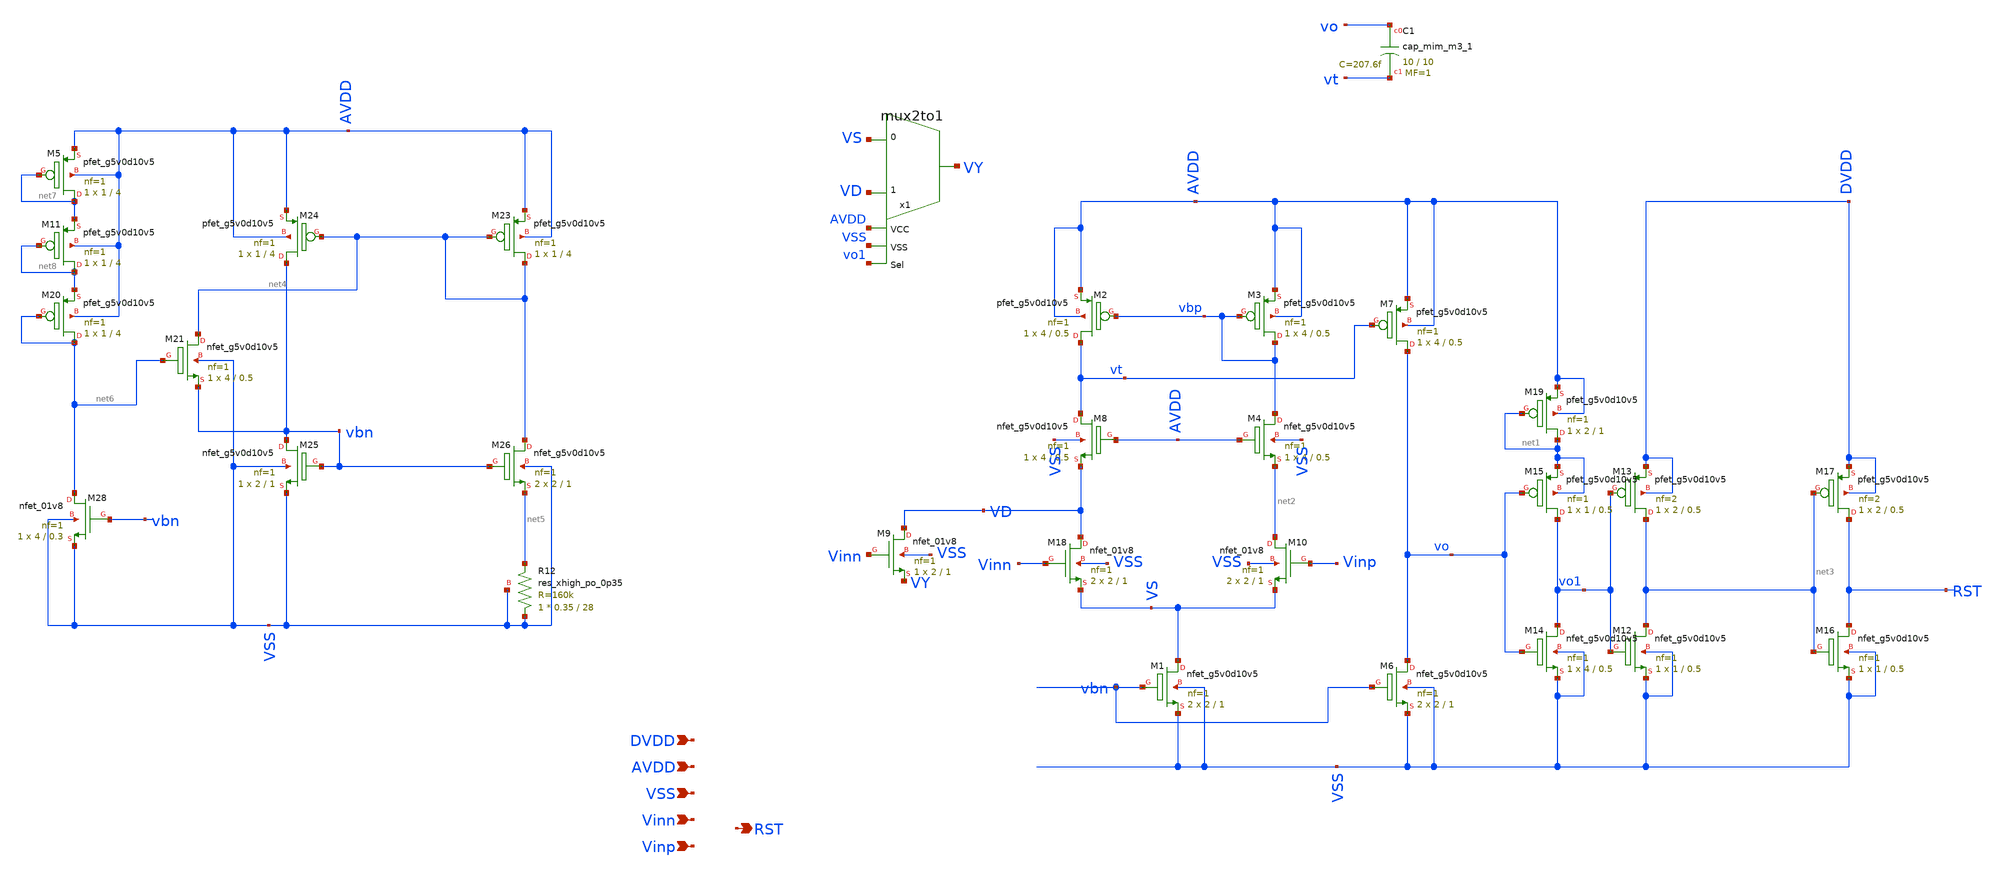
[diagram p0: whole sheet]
** sch_path: xschem/comparator_final_dev.sch
**.subckt comparator_final_dev AVDD RST VSS Vinn Vinp DVDD
*.ipin AVDD
*.opin RST
*.ipin VSS
*.ipin Vinn
*.ipin Vinp
*.ipin DVDD
XM1 VS vbn VSS VSS sky130_fd_pr__nfet_g5v0d10v5 L=1 W=2 nf=1 ad='int((nf+1)/2) * W/nf * 0.29' as='int((nf+2)/2) * W/nf * 0.29'
+ pd='2*int((nf+1)/2) * (W/nf + 0.29)' ps='2*int((nf+2)/2) * (W/nf + 0.29)' nrd='0.29 / W' nrs='0.29 / W'
+ sa=0 sb=0 sd=0 mult=2 m=2
XM3 vbp vbp AVDD AVDD sky130_fd_pr__pfet_g5v0d10v5 L=0.5 W=4 nf=1 ad='int((nf+1)/2) * W/nf * 0.29' as='int((nf+2)/2) * W/nf * 0.29'
+ pd='2*int((nf+1)/2) * (W/nf + 0.29)' ps='2*int((nf+2)/2) * (W/nf + 0.29)' nrd='0.29 / W' nrs='0.29 / W'
+ sa=0 sb=0 sd=0 mult=1 m=1
XM2 vt vbp AVDD AVDD sky130_fd_pr__pfet_g5v0d10v5 L=0.5 W=4 nf=1 ad='int((nf+1)/2) * W/nf * 0.29' as='int((nf+2)/2) * W/nf * 0.29'
+ pd='2*int((nf+1)/2) * (W/nf + 0.29)' ps='2*int((nf+2)/2) * (W/nf + 0.29)' nrd='0.29 / W' nrs='0.29 / W'
+ sa=0 sb=0 sd=0 mult=1 m=1
XM7 vo vt AVDD AVDD sky130_fd_pr__pfet_g5v0d10v5 L=0.5 W=4 nf=1 ad='int((nf+1)/2) * W/nf * 0.29' as='int((nf+2)/2) * W/nf * 0.29'
+ pd='2*int((nf+1)/2) * (W/nf + 0.29)' ps='2*int((nf+2)/2) * (W/nf + 0.29)' nrd='0.29 / W' nrs='0.29 / W'
+ sa=0 sb=0 sd=0 mult=1 m=1
x1 VD VS VY AVDD VSS vo1 mux2to1
XM6 vo vbn VSS VSS sky130_fd_pr__nfet_g5v0d10v5 L=1 W=2 nf=1 ad='int((nf+1)/2) * W/nf * 0.29' as='int((nf+2)/2) * W/nf * 0.29'
+ pd='2*int((nf+1)/2) * (W/nf + 0.29)' ps='2*int((nf+2)/2) * (W/nf + 0.29)' nrd='0.29 / W' nrs='0.29 / W'
+ sa=0 sb=0 sd=0 mult=2 m=2
XM14 vo1 vo VSS VSS sky130_fd_pr__nfet_g5v0d10v5 L=0.5 W=4 nf=1 ad='int((nf+1)/2) * W/nf * 0.29' as='int((nf+2)/2) * W/nf * 0.29'
+ pd='2*int((nf+1)/2) * (W/nf + 0.29)' ps='2*int((nf+2)/2) * (W/nf + 0.29)' nrd='0.29 / W' nrs='0.29 / W'
+ sa=0 sb=0 sd=0 mult=1 m=1
XM15 vo1 vo net1 net1 sky130_fd_pr__pfet_g5v0d10v5 L=0.5 W=1 nf=1 ad='int((nf+1)/2) * W/nf * 0.29' as='int((nf+2)/2) * W/nf * 0.29'
+ pd='2*int((nf+1)/2) * (W/nf + 0.29)' ps='2*int((nf+2)/2) * (W/nf + 0.29)' nrd='0.29 / W' nrs='0.29 / W'
+ sa=0 sb=0 sd=0 mult=1 m=1
XM12 net3 vo1 VSS VSS sky130_fd_pr__nfet_g5v0d10v5 L=0.5 W=1 nf=1 ad='int((nf+1)/2) * W/nf * 0.29' as='int((nf+2)/2) * W/nf * 0.29'
+ pd='2*int((nf+1)/2) * (W/nf + 0.29)' ps='2*int((nf+2)/2) * (W/nf + 0.29)' nrd='0.29 / W' nrs='0.29 / W'
+ sa=0 sb=0 sd=0 mult=1 m=1
XM13 net3 vo1 DVDD DVDD sky130_fd_pr__pfet_g5v0d10v5 L=0.5 W=2 nf=2 ad='int((nf+1)/2) * W/nf * 0.29'
+ as='int((nf+2)/2) * W/nf * 0.29' pd='2*int((nf+1)/2) * (W/nf + 0.29)' ps='2*int((nf+2)/2) * (W/nf + 0.29)'
+ nrd='0.29 / W' nrs='0.29 / W' sa=0 sb=0 sd=0 mult=1 m=1
XM16 RST net3 VSS VSS sky130_fd_pr__nfet_g5v0d10v5 L=0.5 W=1 nf=1 ad='int((nf+1)/2) * W/nf * 0.29' as='int((nf+2)/2) * W/nf * 0.29'
+ pd='2*int((nf+1)/2) * (W/nf + 0.29)' ps='2*int((nf+2)/2) * (W/nf + 0.29)' nrd='0.29 / W' nrs='0.29 / W'
+ sa=0 sb=0 sd=0 mult=1 m=1
XM17 RST net3 DVDD DVDD sky130_fd_pr__pfet_g5v0d10v5 L=0.5 W=2 nf=2 ad='int((nf+1)/2) * W/nf * 0.29'
+ as='int((nf+2)/2) * W/nf * 0.29' pd='2*int((nf+1)/2) * (W/nf + 0.29)' ps='2*int((nf+2)/2) * (W/nf + 0.29)'
+ nrd='0.29 / W' nrs='0.29 / W' sa=0 sb=0 sd=0 mult=1 m=1
XM4 vbp AVDD net2 VSS sky130_fd_pr__nfet_g5v0d10v5 L=0.5 W=4 nf=1 ad='int((nf+1)/2) * W/nf * 0.29' as='int((nf+2)/2) * W/nf * 0.29'
+ pd='2*int((nf+1)/2) * (W/nf + 0.29)' ps='2*int((nf+2)/2) * (W/nf + 0.29)' nrd='0.29 / W' nrs='0.29 / W'
+ sa=0 sb=0 sd=0 mult=1 m=1
XM8 vt AVDD VD VSS sky130_fd_pr__nfet_g5v0d10v5 L=0.5 W=4 nf=1 ad='int((nf+1)/2) * W/nf * 0.29' as='int((nf+2)/2) * W/nf * 0.29'
+ pd='2*int((nf+1)/2) * (W/nf + 0.29)' ps='2*int((nf+2)/2) * (W/nf + 0.29)' nrd='0.29 / W' nrs='0.29 / W'
+ sa=0 sb=0 sd=0 mult=1 m=1
XM19 net1 net1 AVDD AVDD sky130_fd_pr__pfet_g5v0d10v5 L=1 W=2 nf=1 ad='int((nf+1)/2) * W/nf * 0.29' as='int((nf+2)/2) * W/nf * 0.29'
+ pd='2*int((nf+1)/2) * (W/nf + 0.29)' ps='2*int((nf+2)/2) * (W/nf + 0.29)' nrd='0.29 / W' nrs='0.29 / W'
+ sa=0 sb=0 sd=0 mult=1 m=1
XM23 net4 net4 AVDD AVDD sky130_fd_pr__pfet_g5v0d10v5 L=4 W=1 nf=1 ad='int((nf+1)/2) * W/nf * 0.29' as='int((nf+2)/2) * W/nf * 0.29'
+ pd='2*int((nf+1)/2) * (W/nf + 0.29)' ps='2*int((nf+2)/2) * (W/nf + 0.29)' nrd='0.29 / W' nrs='0.29 / W'
+ sa=0 sb=0 sd=0 mult=1 m=1
XM24 vbn net4 AVDD AVDD sky130_fd_pr__pfet_g5v0d10v5 L=4 W=1 nf=1 ad='int((nf+1)/2) * W/nf * 0.29' as='int((nf+2)/2) * W/nf * 0.29'
+ pd='2*int((nf+1)/2) * (W/nf + 0.29)' ps='2*int((nf+2)/2) * (W/nf + 0.29)' nrd='0.29 / W' nrs='0.29 / W'
+ sa=0 sb=0 sd=0 mult=1 m=1
XR12 VSS net5 VSS sky130_fd_pr__res_xhigh_po_0p35 L=28 mult=1 m=1
XM25 vbn vbn VSS VSS sky130_fd_pr__nfet_g5v0d10v5 L=1 W=2 nf=1 ad='int((nf+1)/2) * W/nf * 0.29' as='int((nf+2)/2) * W/nf * 0.29'
+ pd='2*int((nf+1)/2) * (W/nf + 0.29)' ps='2*int((nf+2)/2) * (W/nf + 0.29)' nrd='0.29 / W' nrs='0.29 / W'
+ sa=0 sb=0 sd=0 mult=1 m=1
XM26 net4 vbn net5 VSS sky130_fd_pr__nfet_g5v0d10v5 L=1 W=2 nf=1 ad='int((nf+1)/2) * W/nf * 0.29' as='int((nf+2)/2) * W/nf * 0.29'
+ pd='2*int((nf+1)/2) * (W/nf + 0.29)' ps='2*int((nf+2)/2) * (W/nf + 0.29)' nrd='0.29 / W' nrs='0.29 / W'
+ sa=0 sb=0 sd=0 mult=2 m=2
XM28 net6 vbn VSS VSS sky130_fd_pr__nfet_01v8 L=0.3 W=4 nf=1 ad='int((nf+1)/2) * W/nf * 0.29' as='int((nf+2)/2) * W/nf * 0.29'
+ pd='2*int((nf+1)/2) * (W/nf + 0.29)' ps='2*int((nf+2)/2) * (W/nf + 0.29)' nrd='0.29 / W' nrs='0.29 / W'
+ sa=0 sb=0 sd=0 mult=1 m=1
XM18 VD Vinn VS VSS sky130_fd_pr__nfet_01v8 L=1 W=2 nf=1 ad='int((nf+1)/2) * W/nf * 0.29' as='int((nf+2)/2) * W/nf * 0.29'
+ pd='2*int((nf+1)/2) * (W/nf + 0.29)' ps='2*int((nf+2)/2) * (W/nf + 0.29)' nrd='0.29 / W' nrs='0.29 / W'
+ sa=0 sb=0 sd=0 mult=2 m=2
XM9 VD Vinn VY VSS sky130_fd_pr__nfet_01v8 L=1 W=2 nf=1 ad='int((nf+1)/2) * W/nf * 0.29' as='int((nf+2)/2) * W/nf * 0.29'
+ pd='2*int((nf+1)/2) * (W/nf + 0.29)' ps='2*int((nf+2)/2) * (W/nf + 0.29)' nrd='0.29 / W' nrs='0.29 / W'
+ sa=0 sb=0 sd=0 mult=1 m=1
XM10 net2 Vinp VS VSS sky130_fd_pr__nfet_01v8 L=1 W=2 nf=1 ad='int((nf+1)/2) * W/nf * 0.29' as='int((nf+2)/2) * W/nf * 0.29'
+ pd='2*int((nf+1)/2) * (W/nf + 0.29)' ps='2*int((nf+2)/2) * (W/nf + 0.29)' nrd='0.29 / W' nrs='0.29 / W'
+ sa=0 sb=0 sd=0 mult=2 m=2
XM5 net7 net7 AVDD AVDD sky130_fd_pr__pfet_g5v0d10v5 L=4 W=1 nf=1 ad='int((nf+1)/2) * W/nf * 0.29' as='int((nf+2)/2) * W/nf * 0.29'
+ pd='2*int((nf+1)/2) * (W/nf + 0.29)' ps='2*int((nf+2)/2) * (W/nf + 0.29)' nrd='0.29 / W' nrs='0.29 / W'
+ sa=0 sb=0 sd=0 mult=1 m=1
XM11 net8 net8 net7 AVDD sky130_fd_pr__pfet_g5v0d10v5 L=4 W=1 nf=1 ad='int((nf+1)/2) * W/nf * 0.29' as='int((nf+2)/2) * W/nf * 0.29'
+ pd='2*int((nf+1)/2) * (W/nf + 0.29)' ps='2*int((nf+2)/2) * (W/nf + 0.29)' nrd='0.29 / W' nrs='0.29 / W'
+ sa=0 sb=0 sd=0 mult=1 m=1
XM20 net6 net6 net8 AVDD sky130_fd_pr__pfet_g5v0d10v5 L=4 W=1 nf=1 ad='int((nf+1)/2) * W/nf * 0.29' as='int((nf+2)/2) * W/nf * 0.29'
+ pd='2*int((nf+1)/2) * (W/nf + 0.29)' ps='2*int((nf+2)/2) * (W/nf + 0.29)' nrd='0.29 / W' nrs='0.29 / W'
+ sa=0 sb=0 sd=0 mult=1 m=1
XM21 net4 net6 vbn VSS sky130_fd_pr__nfet_g5v0d10v5 L=0.5 W=4 nf=1 ad='int((nf+1)/2) * W/nf * 0.29' as='int((nf+2)/2) * W/nf * 0.29'
+ pd='2*int((nf+1)/2) * (W/nf + 0.29)' ps='2*int((nf+2)/2) * (W/nf + 0.29)' nrd='0.29 / W' nrs='0.29 / W'
+ sa=0 sb=0 sd=0 mult=1 m=1
XC1 vo vt sky130_fd_pr__cap_mim_m3_1 W=10 L=10 MF=1 m=1
**.ends
.end
